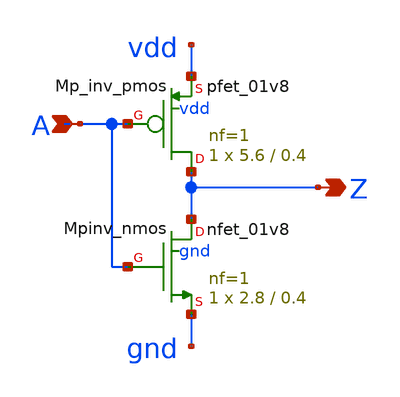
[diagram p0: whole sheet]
** sch_path: sram_2_64_scn4m/pinv_8.sch
**.subckt pinv_8 A Z
*.ipin A
*.opin Z
XMpinv_nmos Z A gnd gnd sky130_fd_pr__nfet_01v8 L=0.4 W=2.8 nf=1 ad='int((nf+1)/2) * W/nf * 0.29' as='int((nf+2)/2) * W/nf * 0.29'
+ pd='2*int((nf+1)/2) * (W/nf + 0.29)' ps='2*int((nf+2)/2) * (W/nf + 0.29)' nrd='0.29 / W' nrs='0.29 / W'
+ sa=0 sb=0 sd=0 mult=1 m=1
XMp_inv_pmos Z A vdd vdd sky130_fd_pr__pfet_01v8 L=0.4 W=5.6 nf=1 ad='int((nf+1)/2) * W/nf * 0.29' as='int((nf+2)/2) * W/nf * 0.29'
+ pd='2*int((nf+1)/2) * (W/nf + 0.29)' ps='2*int((nf+2)/2) * (W/nf + 0.29)' nrd='0.29 / W' nrs='0.29 / W'
+ sa=0 sb=0 sd=0 mult=1 m=1
**.ends
.end
